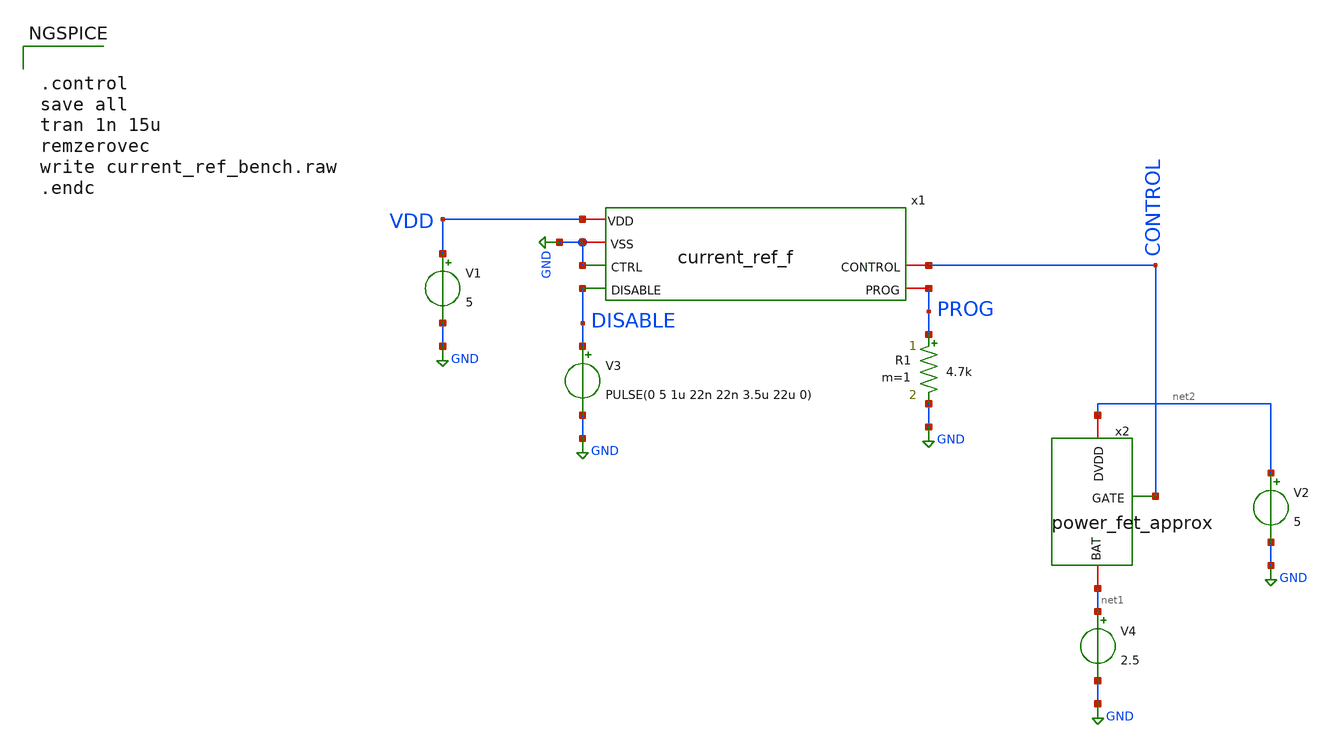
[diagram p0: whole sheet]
** sch_path: analog/xschem/current_ref_bench.sch
**.subckt current_ref_bench
V1 VDD GND 5
V4 net1 GND 2.5
V2 net2 GND 5
R1 PROG GND 4.7k m=1
V3 DISABLE GND PULSE(0 5 1u 22n 22n 3.5u 22u 0)
x2 net2 CONTROL net1 power_fet_approx
x1 VDD GND GND DISABLE CONTROL PROG current_ref_f
**** begin user architecture code


.control
save all
tran 1n 15u
remzerovec
write current_ref_bench.raw
.endc



.include $::180MCU_MODELS/design.ngspice
.lib $::180MCU_MODELS/sm141064.ngspice typical
.lib $::180MCU_MODELS/sm141064.ngspice res_typical
.lib $::180MCU_MODELS/sm141064.ngspice diode_typical
.lib $::180MCU_MODELS/sm141064.ngspice mimcap_typical
.lib $::180MCU_MODELS/sm141064.ngspice cap_mim
.include /foss/designs/charger/xschem/extracted/current_ref_f.spice

**** end user architecture code
**.ends

* expanding   symbol:  power_fet_approx.sym # of pins=3
** sym_path: analog/xschem/power_fet_approx.sym
** sch_path: analog/xschem/power_fet_approx.sch
.subckt power_fet_approx DVDD GATE BAT
*.iopin DVDD
*.iopin BAT
*.ipin GATE
XM1 BAT GATE DVDD DVDD pfet_06v0 L=2u W=46.72u nf=10 ad='int((nf+1)/2) * W/nf * 0.18u' as='int((nf+2)/2) * W/nf * 0.18u'
+ pd='2*int((nf+1)/2) * (W/nf + 0.18u)' ps='2*int((nf+2)/2) * (W/nf + 0.18u)' nrd='0.18u / W' nrs='0.18u / W'
+ sa=0 sb=0 sd=0 m=7920
XM2 BAT GATE DVDD DVDD pfet_06v0 L=2u W=76.465u nf=10 ad='int((nf+1)/2) * W/nf * 0.18u' as='int((nf+2)/2) * W/nf * 0.18u'
+ pd='2*int((nf+1)/2) * (W/nf + 0.18u)' ps='2*int((nf+2)/2) * (W/nf + 0.18u)' nrd='0.18u / W' nrs='0.18u / W'
+ sa=0 sb=0 sd=0 m=7260
.ends

.GLOBAL GND
.end
